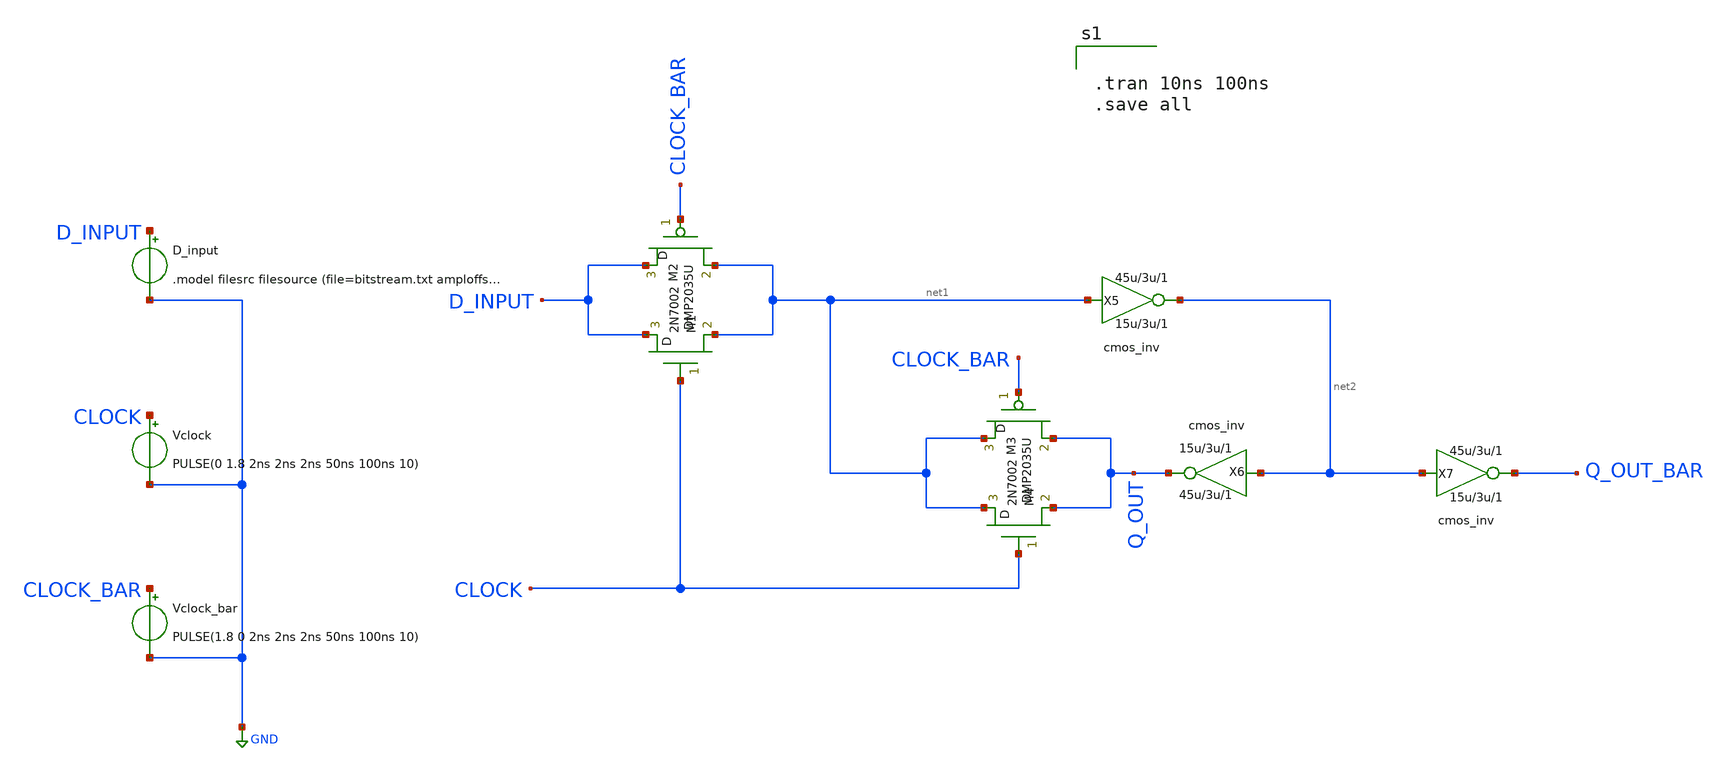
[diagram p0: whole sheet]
** sch_path: Analog_design_files/INV_EXP/dff_tg.sch
* StefanSchippers/xschem/xschem_library/examples/cmos_inv.sch:
* Copyright (C) 1998-2023 Stefan Frederik Schippers
* This program is free software; you can redistribute it and/or modify
* it under the terms of the GNU General Public License as published by
* the Free Software Foundation; either version 2 of the License, or
* (at your option) any later version.
**.subckt dff_tg
X5 net2 net1 cmos_inv WN=15u WP=45u LLN=3u LLP=3u m=1
X6 Q_OUT net2 cmos_inv WN=15u WP=45u LLN=3u LLP=3u m=1
X7 Q_OUT_BAR net2 cmos_inv WN=15u WP=45u LLN=3u LLP=3u m=1
Vclock CLOCK GND PULSE(0 1.8 2ns 2ns 2ns 50ns 100ns 10)
Vclock_bar CLOCK_BAR GND PULSE(1.8 0 2ns 2ns 2ns 50ns 100ns 10)
D_input D_INPUT GND .model filesrc filesource (file=bitstream.txt amploffset=[0] amplscale=[1]
+ timeoffset=0 timescale=1 timerelative=false amplstep=true)
M1 D_INPUT CLOCK net1 M2N7002 m=1
M2 D_INPUT CLOCK_BAR net1 DMP2035U m=1
M3 net1 CLOCK_BAR Q_OUT DMP2035U m=1
M4 net1 CLOCK Q_OUT M2N7002 m=1
**** begin user architecture code


.tran 10ns 100ns
.save all


**** end user architecture code
**.ends

* expanding   symbol:  cmos_inv.sym # of pins=2
** sym_path: cmos_inv.sym
** sch_path: cmos_inv.sch
.subckt cmos_inv Z A  WN=15u WP=45u LLN=3u LLP=3u
*.opin Z
*.ipin A
M2 net1 A VDD VDD p w=WP l=LLP m=1
M1 D A 0 0 n w=WN l=LLN m=1
R1 net2 D 10 m=1
V1 net1 D 0
.save i(v1)
Vmeas net2 Z 0
.save i(vmeas)
.ends

.GLOBAL GND
.GLOBAL VDD
.end
